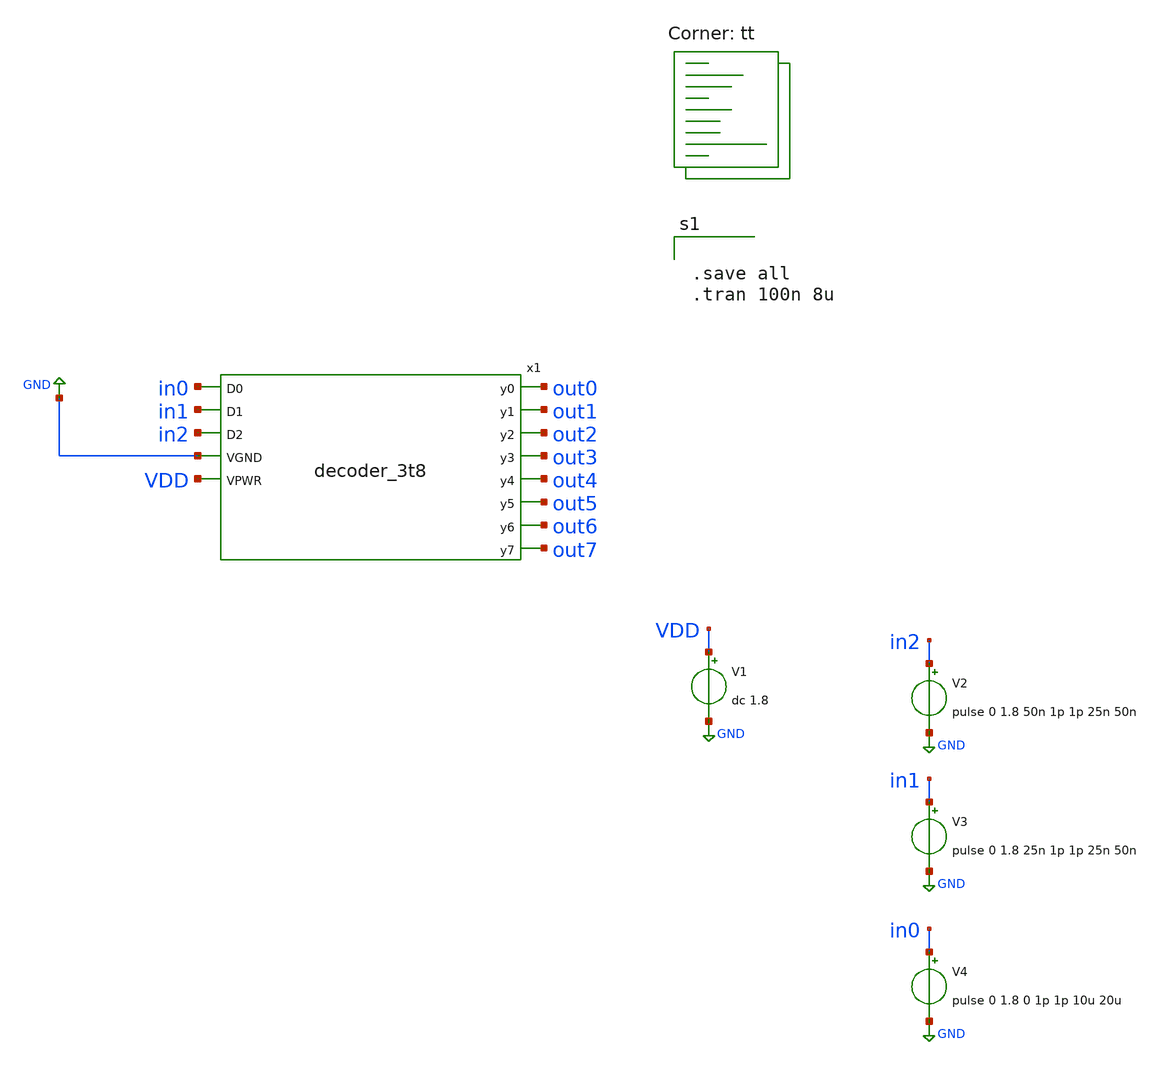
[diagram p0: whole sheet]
** sch_path: xschem/decoder_tb.sch
**.subckt decoder_tb
x1 in0 in1 in2 GND VDD out0 out1 out2 out3 out4 out5 out6 out7 decoder_3t8
V1 VDD GND dc 1.8
V2 in2 GND pulse 0 1.8 50n 1p 1p 25n 50n
V3 in1 GND pulse 0 1.8 25n 1p 1p 25n 50n
V4 in0 GND pulse 0 1.8 0 1p 1p 10u 20u
**** begin user architecture code
.lib $::SKYWATER_MODELS/sky130.lib.spice tt


.save all
.tran 100n 8u



** opencircuitdesign pdks install
.include $::SKYWATER_STDCELLS/sky130_fd_sc_hd.spice


**** end user architecture code
**.ends

* expanding   symbol:  decoder_3t8.sym # of pins=13
** sym_path: xschem/decoder_3t8.sym
** sch_path: xschem/decoder_3t8.sch
.subckt decoder_3t8 D0 D1 D2 VGND VPWR y0 y1 y2 y3 y4 y5 y6 y7
*.ipin D0
*.ipin D1
*.ipin D2
*.ipin VGND
*.ipin VPWR
*.opin y0
*.opin y1
*.opin y2
*.opin y3
*.opin y4
*.opin y5
*.opin y6
*.opin y7
X_0_ net3 net2 net1 VGND VGND VPWR VPWR net5 sky130_fd_sc_hd__nor3b_1
X_1_ net3 net1 net2 VGND VGND VPWR VPWR net6 sky130_fd_sc_hd__nor3b_1
X_2_ net3 net2 net1 VGND VGND VPWR VPWR net7 sky130_fd_sc_hd__and3b_1
X_3_ net2 net1 net3 VGND VGND VPWR VPWR net8 sky130_fd_sc_hd__nor3b_1
X_4_ net2 net1 net3 VGND VGND VPWR VPWR net9 sky130_fd_sc_hd__and3b_1
X_5_ net1 net2 net3 VGND VGND VPWR VPWR net10 sky130_fd_sc_hd__and3b_1
X_6_ net3 net2 net1 VGND VGND VPWR VPWR net11 sky130_fd_sc_hd__and3_1
X_7_ net3 net2 net1 VGND VGND VPWR VPWR net4 sky130_fd_sc_hd__nor3_1
Xinput1 D0 VGND VGND VPWR VPWR net1 sky130_fd_sc_hd__clkbuf_2
Xinput2 D1 VGND VGND VPWR VPWR net2 sky130_fd_sc_hd__clkbuf_2
Xinput3 D2 VGND VGND VPWR VPWR net3 sky130_fd_sc_hd__clkbuf_2
Xoutput10 net10 VGND VGND VPWR VPWR y6 sky130_fd_sc_hd__buf_12
Xoutput11 net11 VGND VGND VPWR VPWR y7 sky130_fd_sc_hd__buf_12
Xoutput4 net4 VGND VGND VPWR VPWR y0 sky130_fd_sc_hd__buf_12
Xoutput5 net5 VGND VGND VPWR VPWR y1 sky130_fd_sc_hd__buf_12
Xoutput6 net6 VGND VGND VPWR VPWR y2 sky130_fd_sc_hd__buf_12
Xoutput7 net7 VGND VGND VPWR VPWR y3 sky130_fd_sc_hd__buf_12
Xoutput8 net8 VGND VGND VPWR VPWR y4 sky130_fd_sc_hd__buf_12
Xoutput9 net9 VGND VGND VPWR VPWR y5 sky130_fd_sc_hd__buf_12
.ends

.GLOBAL GND
.end
